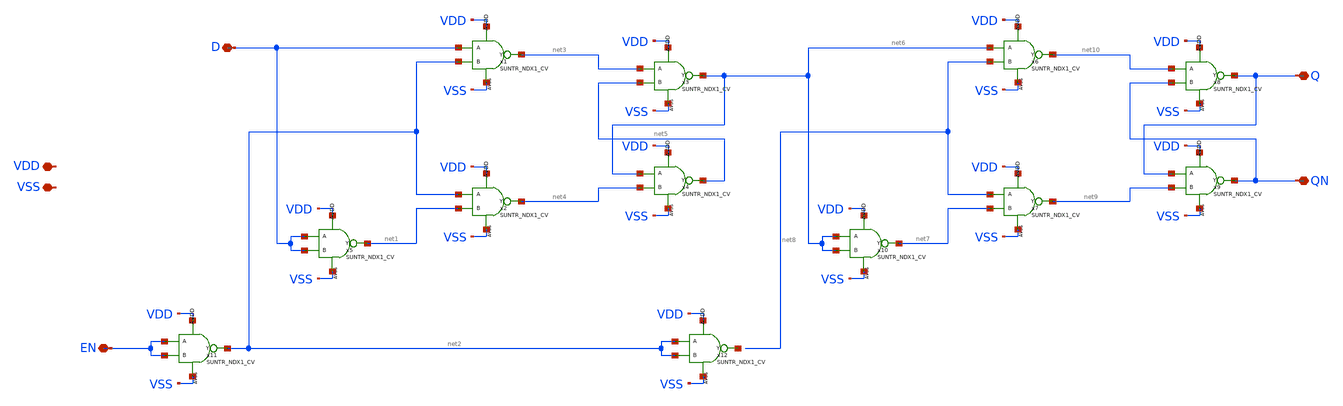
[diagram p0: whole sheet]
** sch_path: design/CNR_GR03_SKY130NM/DFF.sch
**.subckt DFF VDD VSS D Q EN QN
*.iopin VDD
*.iopin VSS
*.iopin D
*.iopin Q
*.iopin EN
*.iopin QN
x1 D net2 net3 VDD VSS SUNTR_NDX1_CV
x2 net2 net1 net4 VDD VSS SUNTR_NDX1_CV
x3 net3 net5 net6 VDD VSS SUNTR_NDX1_CV
x4 net6 net4 net5 VDD VSS SUNTR_NDX1_CV
x5 D D net1 VDD VSS SUNTR_NDX1_CV
x6 net6 net8 net10 VDD VSS SUNTR_NDX1_CV
x7 net8 net7 net9 VDD VSS SUNTR_NDX1_CV
x8 net10 QN Q VDD VSS SUNTR_NDX1_CV
x9 Q net9 QN VDD VSS SUNTR_NDX1_CV
x10 net6 net6 net7 VDD VSS SUNTR_NDX1_CV
x11 EN EN net2 VDD VSS SUNTR_NDX1_CV
x12 net2 net2 net11 VDD VSS SUNTR_NDX1_CV
**.ends
.end
